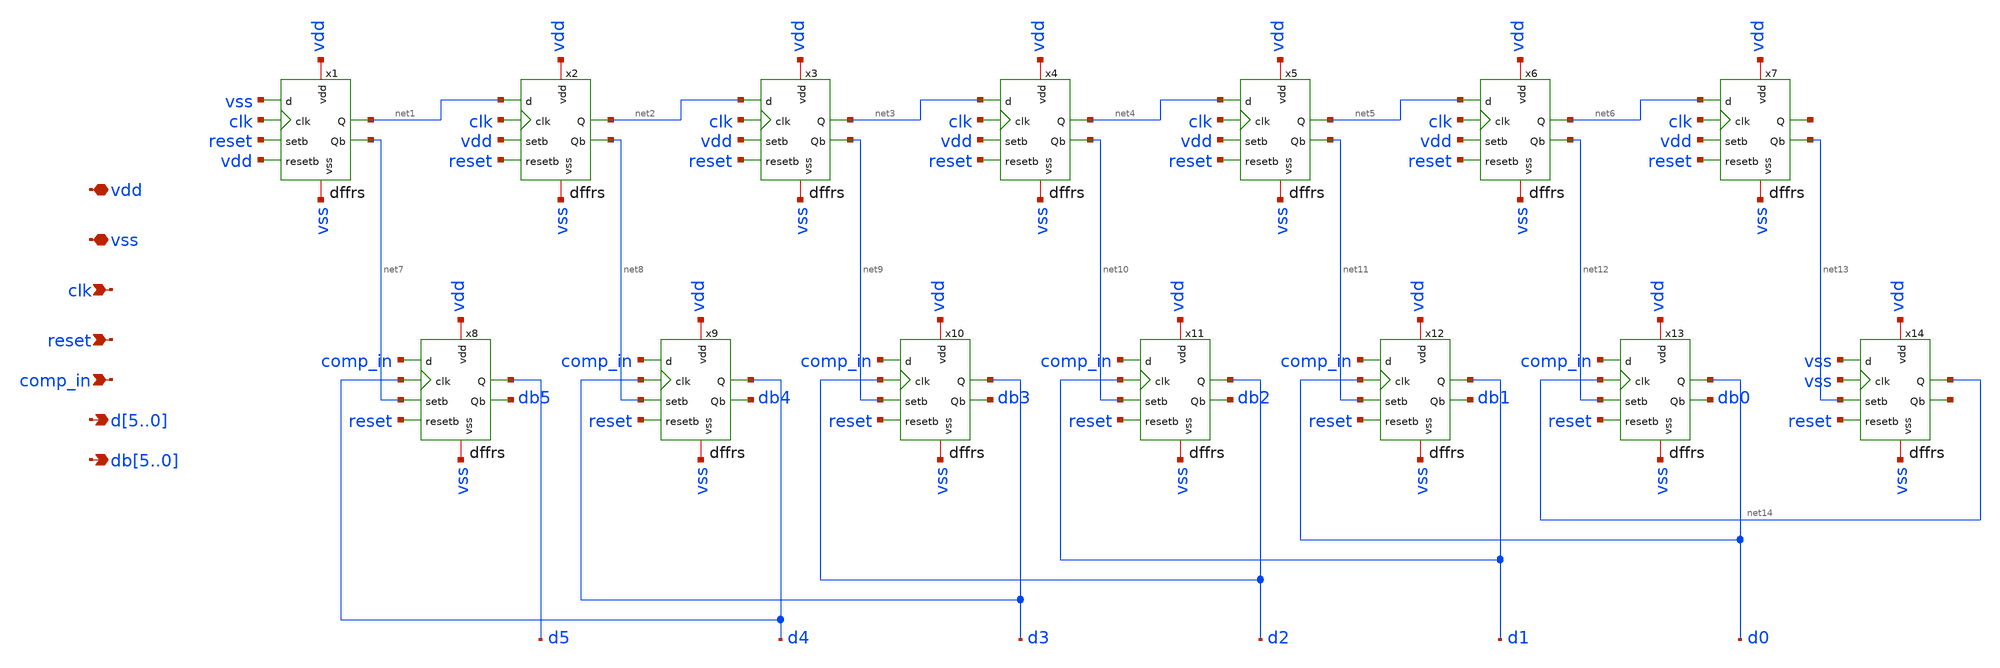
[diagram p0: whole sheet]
** sch_path: designs/FinalBlocksLayout/SARlogic/SARlogic.sch
**.subckt SARlogic comp_in vdd vss clk reset d5,d4,d3,d2,d1,d0 db5,db4,db3,db2,db1,db0
*.ipin comp_in
*.iopin vdd
*.iopin vss
*.ipin clk
*.ipin reset
*.opin d5,d4,d3,d2,d1,d0
*.opin db5,db4,db3,db2,db1,db0
x1 vdd vss vss clk reset vdd net1 net7 dffrs
x2 vdd vss net1 clk vdd reset net2 net8 dffrs
x3 vdd vss net2 clk vdd reset net3 net9 dffrs
x4 vdd vss net3 clk vdd reset net4 net10 dffrs
x5 vdd vss net4 clk vdd reset net5 net11 dffrs
x6 vdd vss net5 clk vdd reset net6 net12 dffrs
x7 vdd vss net6 clk vdd reset net15 net13 dffrs
x8 vdd vss comp_in d4 net7 reset d5 db5 dffrs
x9 vdd vss comp_in d3 net8 reset d4 db4 dffrs
x10 vdd vss comp_in d2 net9 reset d3 db3 dffrs
x11 vdd vss comp_in d1 net10 reset d2 db2 dffrs
x12 vdd vss comp_in d0 net11 reset d1 db1 dffrs
x13 vdd vss comp_in net14 net12 reset d0 db0 dffrs
x14 vdd vss vss vss net13 reset net14 net16 dffrs
**.ends
.end
